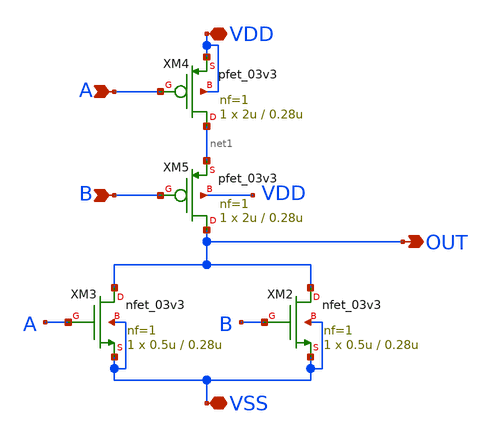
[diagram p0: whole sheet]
** sch_path: SCOP_INPUT_AND_MUX_PAKISTAN_03/Xschem/Logic_Gates/NOR.sch
**.subckt NOR VDD VSS OUT A B
*.iopin VDD
*.iopin VSS
*.opin OUT
*.ipin A
*.ipin B
XM2 OUT B VSS VSS nfet_03v3 L=0.28u W=0.5u nf=1 ad='int((nf+1)/2) * W/nf * 0.18u' as='int((nf+2)/2) * W/nf * 0.18u'
+ pd='2*int((nf+1)/2) * (W/nf + 0.18u)' ps='2*int((nf+2)/2) * (W/nf + 0.18u)' nrd='0.18u / W' nrs='0.18u / W'
+ sa=0 sb=0 sd=0 m=1
XM3 OUT A VSS VSS nfet_03v3 L=0.28u W=0.5u nf=1 ad='int((nf+1)/2) * W/nf * 0.18u' as='int((nf+2)/2) * W/nf * 0.18u'
+ pd='2*int((nf+1)/2) * (W/nf + 0.18u)' ps='2*int((nf+2)/2) * (W/nf + 0.18u)' nrd='0.18u / W' nrs='0.18u / W'
+ sa=0 sb=0 sd=0 m=1
XM4 net1 A VDD VDD pfet_03v3 L=0.28u W=2u nf=1 ad='int((nf+1)/2) * W/nf * 0.18u' as='int((nf+2)/2) * W/nf * 0.18u'
+ pd='2*int((nf+1)/2) * (W/nf + 0.18u)' ps='2*int((nf+2)/2) * (W/nf + 0.18u)' nrd='0.18u / W' nrs='0.18u / W'
+ sa=0 sb=0 sd=0 m=1
XM5 OUT B net1 VDD pfet_03v3 L=0.28u W=2u nf=1 ad='int((nf+1)/2) * W/nf * 0.18u' as='int((nf+2)/2) * W/nf * 0.18u'
+ pd='2*int((nf+1)/2) * (W/nf + 0.18u)' ps='2*int((nf+2)/2) * (W/nf + 0.18u)' nrd='0.18u / W' nrs='0.18u / W'
+ sa=0 sb=0 sd=0 m=1
**.ends
.end
